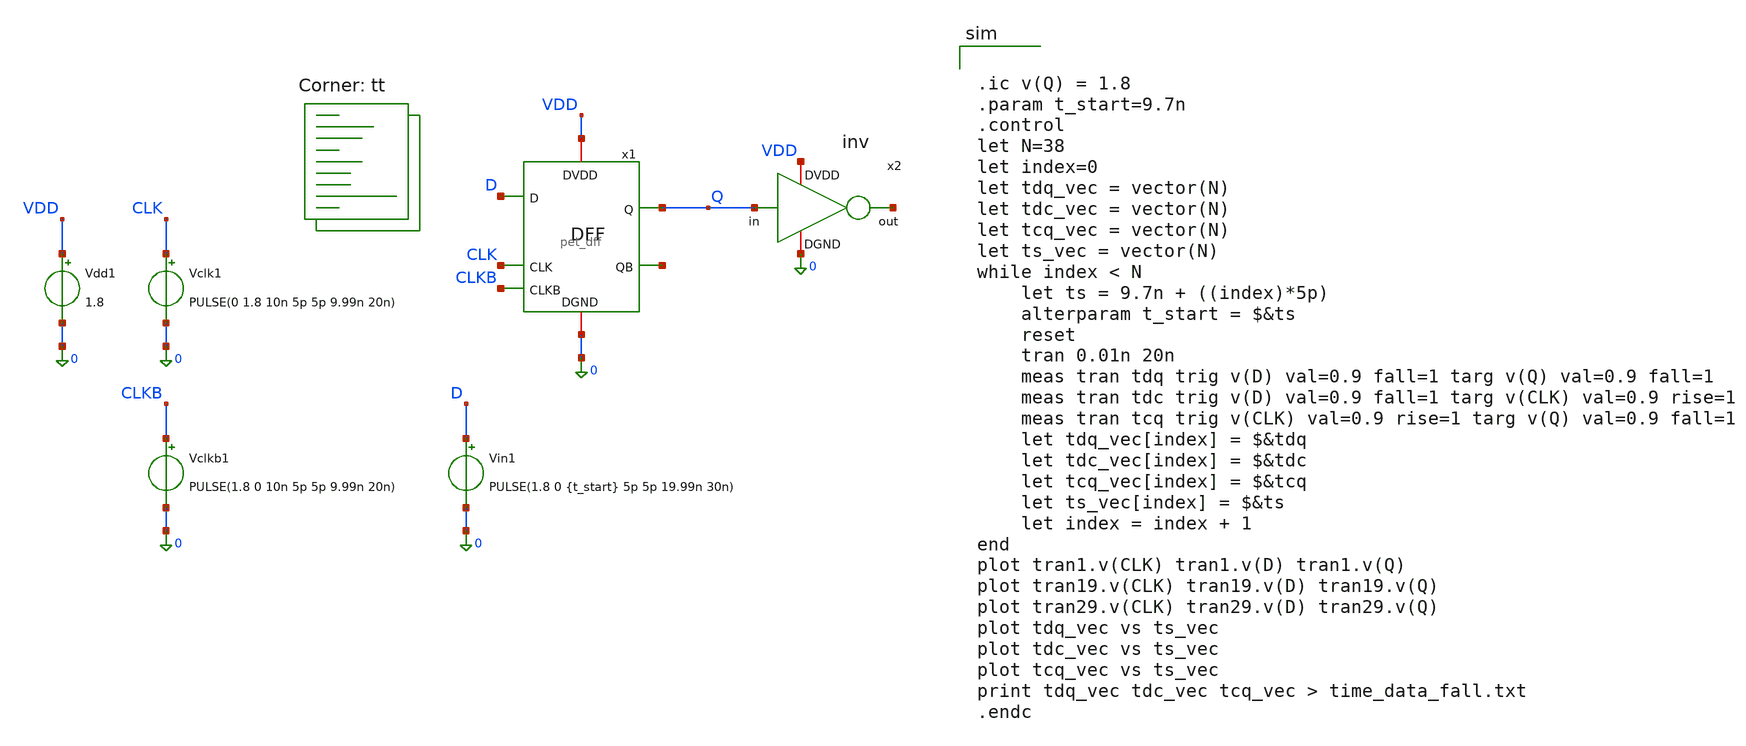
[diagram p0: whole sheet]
** sch_path: tutorial-6/source/pet_dff_tb1_fall.sch
**.subckt pet_dff_tb1_fall
Vdd1 VDD 0 1.8
Vclk1 CLK 0 PULSE(0 1.8 10n 5p 5p 9.99n 20n)
Vclkb1 CLKB 0 PULSE(1.8 0 10n 5p 5p 9.99n 20n)
Vin1 D 0 PULSE(1.8 0 {t_start} 5p 5p 19.99n 30n)
x1 CLKB CLK D Q VDD 0 net1 pet_dff
x2 VDD Q net2 0 inv
**** begin user architecture code
.lib $::SKYWATER_MODELS/sky130.lib.spice tt


.ic v(Q) = 1.8
.param t_start=9.7n
.control
let N=38
let index=0
let tdq_vec = vector(N)
let tdc_vec = vector(N)
let tcq_vec = vector(N)
let ts_vec = vector(N)
while index < N
	let ts = 9.7n + ((index)*5p)
	alterparam t_start = $&ts
	reset
	tran 0.01n 20n
	meas tran tdq trig v(D) val=0.9 fall=1 targ v(Q) val=0.9 fall=1
	meas tran tdc trig v(D) val=0.9 fall=1 targ v(CLK) val=0.9 rise=1
	meas tran tcq trig v(CLK) val=0.9 rise=1 targ v(Q) val=0.9 fall=1
	let tdq_vec[index] = $&tdq
	let tdc_vec[index] = $&tdc
	let tcq_vec[index] = $&tcq
	let ts_vec[index] = $&ts
	let index = index + 1
end
plot tran1.v(CLK) tran1.v(D) tran1.v(Q)
plot tran19.v(CLK) tran19.v(D) tran19.v(Q)
plot tran29.v(CLK) tran29.v(D) tran29.v(Q)
plot tdq_vec vs ts_vec
plot tdc_vec vs ts_vec
plot tcq_vec vs ts_vec
print tdq_vec tdc_vec tcq_vec > time_data_fall.txt
.endc

**** end user architecture code
**.ends

* expanding   symbol:  pet_dff.sym # of pins=7
** sym_path: tutorial-6/source/pet_dff.sym
** sch_path: tutorial-6/source/pet_dff.sch
.subckt pet_dff CLKB CLK D Q DVDD DGND QB
*.ipin D
*.opin Q
*.ipin CLK
*.ipin CLKB
*.iopin DVDD
*.iopin DGND
*.opin QB
XM1 net1 CLK net2 DGND sky130_fd_pr__nfet_01v8 L=0.15 W=0.42 nf=1 ad='int((nf+1)/2) * W/nf * 0.29' as='int((nf+2)/2) * W/nf * 0.29'
+ pd='2*int((nf+1)/2) * (W/nf + 0.29)' ps='2*int((nf+2)/2) * (W/nf + 0.29)' nrd='0.29 / W' nrs='0.29 / W'
+ sa=0 sb=0 sd=0 mult=1 m=1
XM2 net2 CLKB net1 DVDD sky130_fd_pr__pfet_01v8 L=0.15 W=0.42 nf=1 ad='int((nf+1)/2) * W/nf * 0.29' as='int((nf+2)/2) * W/nf * 0.29'
+ pd='2*int((nf+1)/2) * (W/nf + 0.29)' ps='2*int((nf+2)/2) * (W/nf + 0.29)' nrd='0.29 / W' nrs='0.29 / W'
+ sa=0 sb=0 sd=0 mult=1 m=1
XM3 net3 CLKB net2 DGND sky130_fd_pr__nfet_01v8 L=0.15 W=0.42 nf=1 ad='int((nf+1)/2) * W/nf * 0.29' as='int((nf+2)/2) * W/nf * 0.29'
+ pd='2*int((nf+1)/2) * (W/nf + 0.29)' ps='2*int((nf+2)/2) * (W/nf + 0.29)' nrd='0.29 / W' nrs='0.29 / W'
+ sa=0 sb=0 sd=0 mult=1 m=1
XM4 net2 CLK net3 DVDD sky130_fd_pr__pfet_01v8 L=0.15 W=0.42 nf=1 ad='int((nf+1)/2) * W/nf * 0.29' as='int((nf+2)/2) * W/nf * 0.29'
+ pd='2*int((nf+1)/2) * (W/nf + 0.29)' ps='2*int((nf+2)/2) * (W/nf + 0.29)' nrd='0.29 / W' nrs='0.29 / W'
+ sa=0 sb=0 sd=0 mult=1 m=1
XM5 net5 CLKB QB DGND sky130_fd_pr__nfet_01v8 L=0.15 W=0.42 nf=1 ad='int((nf+1)/2) * W/nf * 0.29' as='int((nf+2)/2) * W/nf * 0.29'
+ pd='2*int((nf+1)/2) * (W/nf + 0.29)' ps='2*int((nf+2)/2) * (W/nf + 0.29)' nrd='0.29 / W' nrs='0.29 / W'
+ sa=0 sb=0 sd=0 mult=1 m=1
XM6 QB CLK net5 DVDD sky130_fd_pr__pfet_01v8 L=0.15 W=0.42 nf=1 ad='int((nf+1)/2) * W/nf * 0.29' as='int((nf+2)/2) * W/nf * 0.29'
+ pd='2*int((nf+1)/2) * (W/nf + 0.29)' ps='2*int((nf+2)/2) * (W/nf + 0.29)' nrd='0.29 / W' nrs='0.29 / W'
+ sa=0 sb=0 sd=0 mult=1 m=1
XM7 net6 CLK QB DGND sky130_fd_pr__nfet_01v8 L=0.15 W=0.42 nf=1 ad='int((nf+1)/2) * W/nf * 0.29' as='int((nf+2)/2) * W/nf * 0.29'
+ pd='2*int((nf+1)/2) * (W/nf + 0.29)' ps='2*int((nf+2)/2) * (W/nf + 0.29)' nrd='0.29 / W' nrs='0.29 / W'
+ sa=0 sb=0 sd=0 mult=1 m=1
XM8 QB CLKB net6 DVDD sky130_fd_pr__pfet_01v8 L=0.15 W=0.42 nf=1 ad='int((nf+1)/2) * W/nf * 0.29' as='int((nf+2)/2) * W/nf * 0.29'
+ pd='2*int((nf+1)/2) * (W/nf + 0.29)' ps='2*int((nf+2)/2) * (W/nf + 0.29)' nrd='0.29 / W' nrs='0.29 / W'
+ sa=0 sb=0 sd=0 mult=1 m=1
x1 DVDD net4 net1 DGND inv
x2 DVDD D net3 DGND inv
x3 DVDD net2 net4 DGND inv
x4 DVDD net7 net5 DGND inv
x5 DVDD net4 net6 DGND inv
x6 DVDD QB Q DGND inv
x7 DVDD QB net7 DGND inv
.ends


* expanding   symbol:  inv.sym # of pins=4
** sym_path: tutorial-6/source/inv.sym
** sch_path: tutorial-6/source/inv.sch
.subckt inv DVDD in out DGND
*.iopin DVDD
*.iopin DGND
*.ipin in
*.opin out
XM1 out in DVDD DVDD sky130_fd_pr__pfet_01v8 L=0.15 W=0.84 nf=1 ad='int((nf+1)/2) * W/nf * 0.29' as='int((nf+2)/2) * W/nf * 0.29'
+ pd='2*int((nf+1)/2) * (W/nf + 0.29)' ps='2*int((nf+2)/2) * (W/nf + 0.29)' nrd='0.29 / W' nrs='0.29 / W'
+ sa=0 sb=0 sd=0 mult=1 m=1
XM2 out in DGND DGND sky130_fd_pr__nfet_01v8 L=0.15 W=0.42 nf=1 ad='int((nf+1)/2) * W/nf * 0.29' as='int((nf+2)/2) * W/nf * 0.29'
+ pd='2*int((nf+1)/2) * (W/nf + 0.29)' ps='2*int((nf+2)/2) * (W/nf + 0.29)' nrd='0.29 / W' nrs='0.29 / W'
+ sa=0 sb=0 sd=0 mult=1 m=1
.ends

.end
